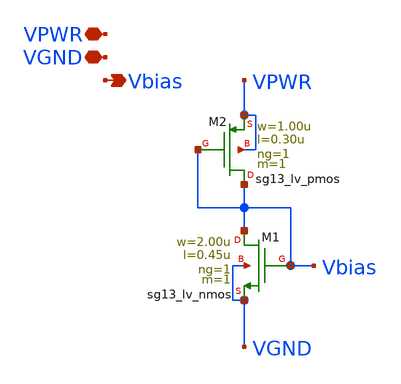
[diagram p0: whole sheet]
** sch_path: xschem/vbias.sch
**.subckt vbias VPWR Vbias VGND
*.iopin VPWR
*.opin Vbias
*.iopin VGND
XM1 Vbias Vbias VGND VGND sg13_lv_nmos w=2.00u l=0.45u ng=1 m=1 mm_ok=1
XM2 Vbias Vbias VPWR VPWR sg13_lv_pmos w=1.00u l=0.30u ng=1 m=1 mm_ok=1
**.ends
.end
